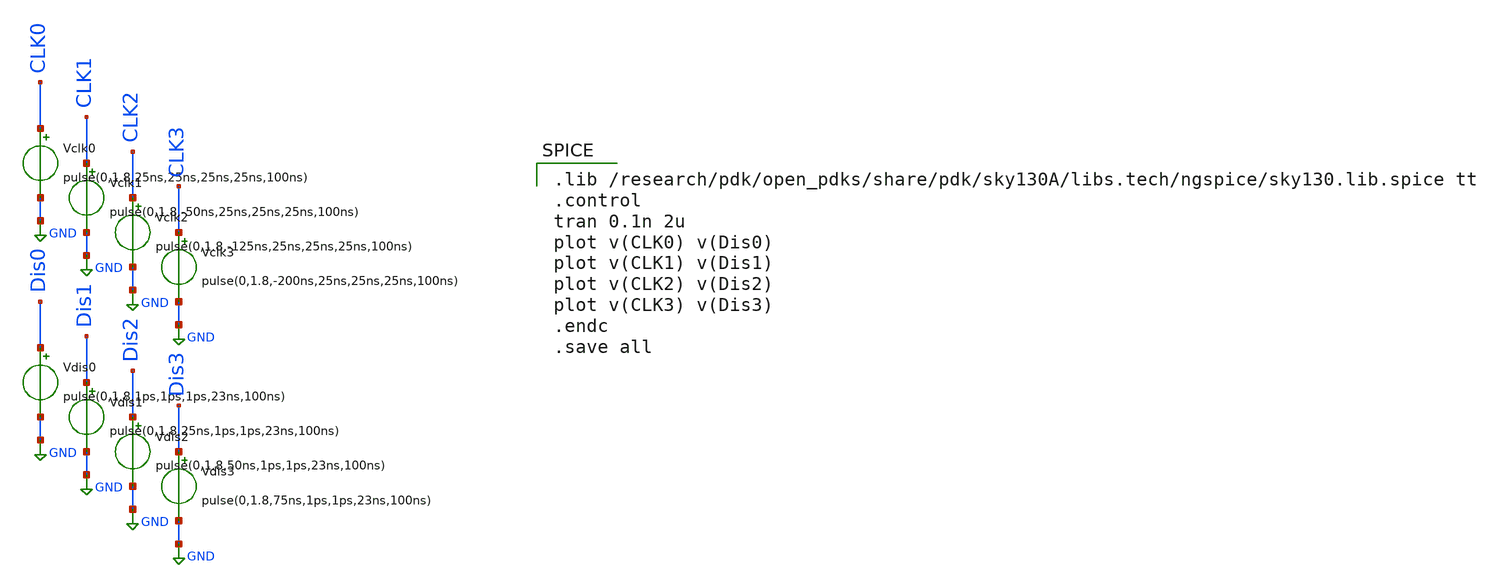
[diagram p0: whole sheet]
** sch_path: skywater_stuff/untitled.sch
**.subckt untitled
Vdis0 Dis0 GND pulse(0,1.8,1ps,1ps,1ps,23ns,100ns)
Vclk0 CLK0 GND pulse(0,1.8,25ns,25ns,25ns,25ns,100ns)
Vdis1 Dis1 GND pulse(0,1.8,25ns,1ps,1ps,23ns,100ns)
Vdis2 Dis2 GND pulse(0,1.8,50ns,1ps,1ps,23ns,100ns)
Vdis3 Dis3 GND pulse(0,1.8,75ns,1ps,1ps,23ns,100ns)
Vclk1 CLK1 GND pulse(0,1.8,-50ns,25ns,25ns,25ns,100ns)
Vclk2 CLK2 GND pulse(0,1.8,-125ns,25ns,25ns,25ns,100ns)
Vclk3 CLK3 GND pulse(0,1.8,-200ns,25ns,25ns,25ns,100ns)
**** begin user architecture code

.lib /research/pdk/open_pdks/share/pdk/sky130A/libs.tech/ngspice/sky130.lib.spice tt
.control
tran 0.1n 2u
plot v(CLK0) v(Dis0)
plot v(CLK1) v(Dis1)
plot v(CLK2) v(Dis2)
plot v(CLK3) v(Dis3)
.endc
.save all

**** end user architecture code
**.ends
.GLOBAL GND
.end
